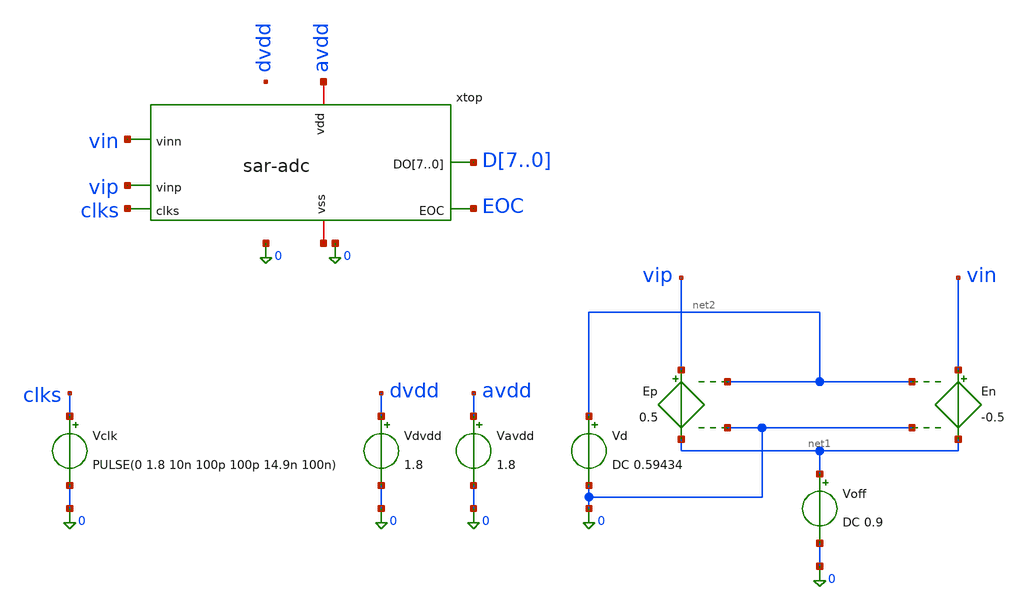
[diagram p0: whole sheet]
** sch_path: xschem/sar-adc_tb/offset_sar-adc_tb.sch
.lib $::SKYWATER_MODELS/sky130.lib.spice tt
.include $::SKYWATER_STDCELLS/sky130_fd_sc_hd.spice

**.subckt offset_sar-adc_tb
xtop vin vip clks D7 D6 D5 D4 D3 D2 D1 D0 avdd net3 EOC sar-adc
Vclk clks 0 PULSE(0 1.8 10n 100p 100p 14.9n 100n)
Vavdd avdd 0 1.8
Vdvdd dvdd 0 1.8
Voff net1 0 DC 0.9
En vin net1 net2 0 -0.5
Ep vip net1 net2 0 0.5
Vd net2 0 DC 0.59434
**** begin user architecture code



.control
 set appendwrite
 foreach vv -0.020 -0.018 -0.016 -0.014 -0.012 -0.010 -0.008 -0.006 -0.004 -0.002
 +        0.000 0.002 0.004 0.006 0.008 0.010 0.012 0.014 0.016 0.018 0.020
   alter Vd = $vv
   tran 20p 30n
   meas tran d7v find v(D7) at=29n
   echo 'SWEEP $vv $&d7v'
   write offset_sar-adc_tb.raw v(D7) v(clks) v(xtop.clkc) v(xtop.ctopp) v(xtop.ctopn)
 +      v(xtop.xcomparator.vtail)
   destroy $curplot
 end
 unset appendwrite
.endc





.param nfft = 64
.param mcyc = 29
.param fs = 10e6
.param fin  = 'mcyc/nfft*fs'     $ 4.53125 MHz
.param amp  = 0.88               $ hampir full-scale single-ended
.param off  = 0.9                $ V_CM
.param namp = '-amp'             $ amplitudo sisi n (fase berlawanan)
.options reltol=1e-4 vntol=1e-8 abstol=1e-14 chgtol=1e-16


**** end user architecture code
**.ends
.end
